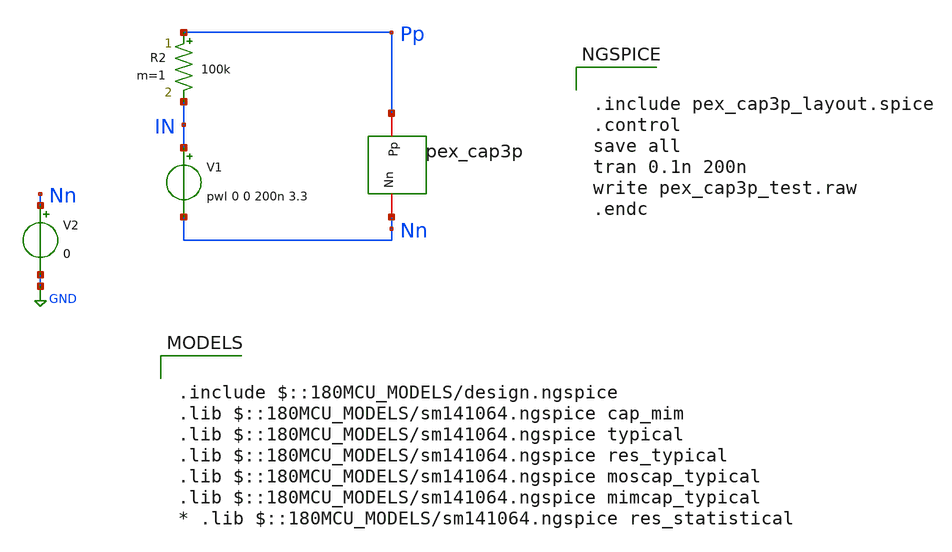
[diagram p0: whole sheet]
** sch_path: Clock_Generator_PAKISTAN_02/Schematics/pex_cap3p_test.sch
**.subckt pex_cap3p_test
V1 IN Nn pwl 0 0 200n 3.3
R2 Pp IN 100k m=1
V2 Nn GND 0
x1 Nn Pp pex_cap3p
**** begin user architecture code

.include $::180MCU_MODELS/design.ngspice
.lib $::180MCU_MODELS/sm141064.ngspice cap_mim
.lib $::180MCU_MODELS/sm141064.ngspice typical
.lib $::180MCU_MODELS/sm141064.ngspice res_typical
.lib $::180MCU_MODELS/sm141064.ngspice moscap_typical
.lib $::180MCU_MODELS/sm141064.ngspice mimcap_typical
* .lib $::180MCU_MODELS/sm141064.ngspice res_statistical



.include pex_cap3p_layout.spice
.control
save all
tran 0.1n 200n
write pex_cap3p_test.raw
.endc


**** end user architecture code
**.ends
.GLOBAL GND
.end
